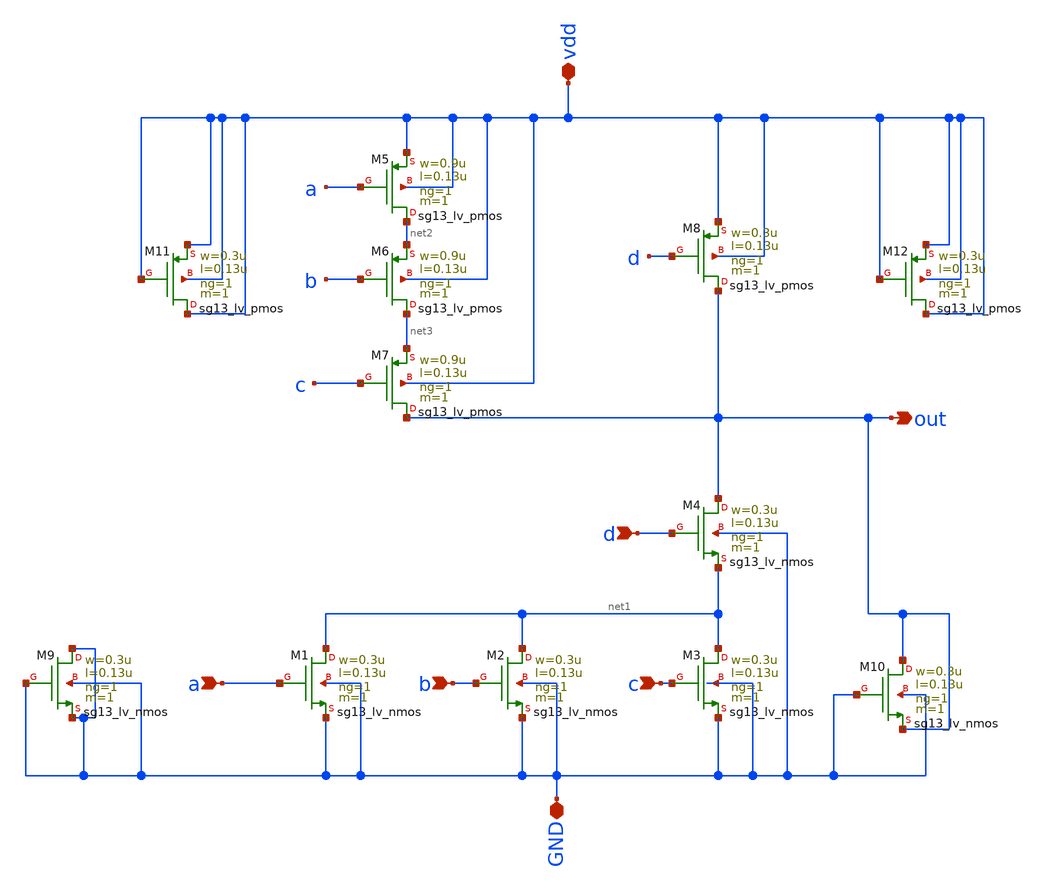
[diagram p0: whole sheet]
** sch_path: projekat/slucaj_2/schematic/funkcija_matching.sch
**.subckt funkcija_matching a b c d vdd GND out
*.ipin a
*.ipin b
*.ipin c
*.ipin d
*.iopin vdd
*.iopin GND
*.opin out
XM1 net1 a GND GND sg13_lv_nmos w=0.3u l=0.13u ng=1 m=1 mm_ok=1
XM2 net1 b GND GND sg13_lv_nmos w=0.3u l=0.13u ng=1 m=1 mm_ok=1
XM3 net1 c GND GND sg13_lv_nmos w=0.3u l=0.13u ng=1 m=1 mm_ok=1
XM4 out d net1 GND sg13_lv_nmos w=0.3u l=0.13u ng=1 m=1 mm_ok=1
XM5 net2 a vdd vdd sg13_lv_pmos w=0.9u l=0.13u ng=1 m=1 mm_ok=1
XM6 net3 b net2 vdd sg13_lv_pmos w=0.9u l=0.13u ng=1 m=1 mm_ok=1
XM7 out c net3 vdd sg13_lv_pmos w=0.9u l=0.13u ng=1 m=1 mm_ok=1
XM8 out d vdd vdd sg13_lv_pmos w=0.3u l=0.13u ng=1 m=1 mm_ok=1
XM9 GND GND GND GND sg13_lv_nmos w=0.3u l=0.13u ng=1 m=1 mm_ok=1
XM10 out GND out GND sg13_lv_nmos w=0.3u l=0.13u ng=1 m=1 mm_ok=1
XM11 vdd vdd vdd vdd sg13_lv_pmos w=0.3u l=0.13u ng=1 m=1 mm_ok=1
XM12 vdd vdd vdd vdd sg13_lv_pmos w=0.3u l=0.13u ng=1 m=1 mm_ok=1
**.ends
.end
